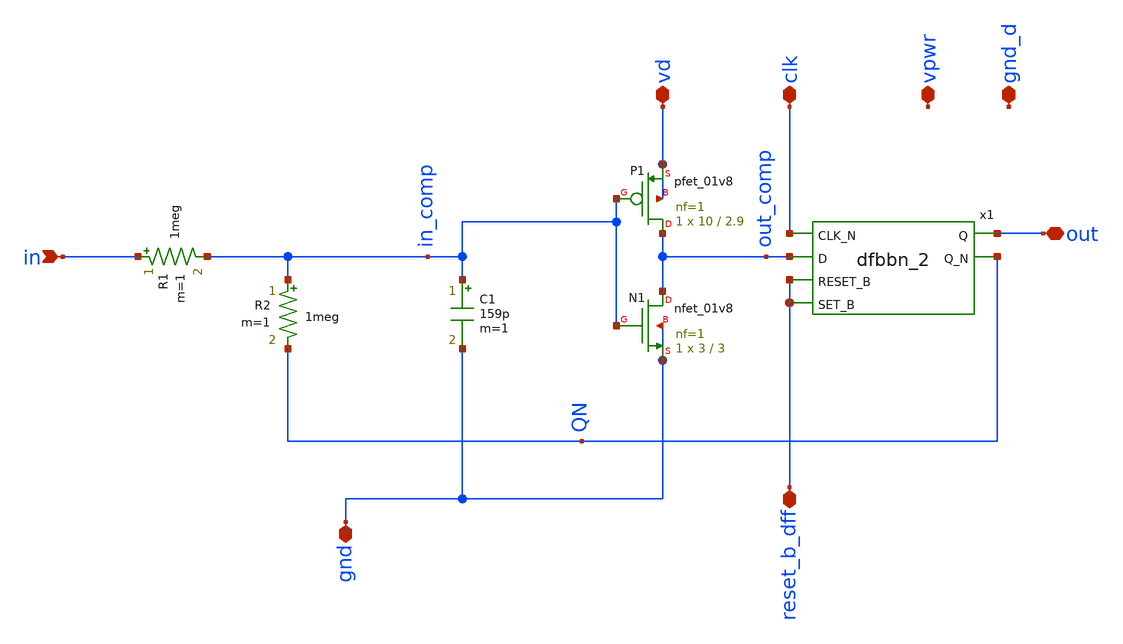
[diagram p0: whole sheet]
** sch_path: mag/sigma-delta_modulator/xschem/sigma-delta-test.sch
* Copyright 2020 Stefan Frederik Schippers
* Licensed under the Apache License, Version 2.0 (the "License");
* you may not use this file except in compliance with the License.
* You may obtain a copy of the License at
* https://www.apache.org/licenses/LICENSE-2.0
* Unless required by applicable law or agreed to in writing, software
* distributed under the License is distributed on an "AS IS" BASIS,
* WITHOUT WARRANTIES OR CONDITIONS OF ANY KIND, either express or implied.
* See the License for the specific language governing permissions and
* limitations under the License.
**.subckt sigma-delta-test in gnd clk out reset_b_dff vpwr gnd_d vd
*.ipin in
*.iopin gnd
*.iopin clk
*.iopin out
*.iopin reset_b_dff
*.iopin vpwr
*.iopin gnd_d
*.iopin vd
XN1 out_comp in_comp gnd gnd sky130_fd_pr__nfet_01v8 L=3 W=3 nf=1 ad='int((nf+1)/2) * W/nf * 0.29' as='int((nf+2)/2) * W/nf * 0.29'
+ pd='2*int((nf+1)/2) * (W/nf + 0.29)' ps='2*int((nf+2)/2) * (W/nf + 0.29)' nrd='0.29 / W' nrs='0.29 / W'
+ sa=0 sb=0 sd=0 mult=1 m=1
XP1 out_comp in_comp vd vd sky130_fd_pr__pfet_01v8 L=2.9 W=10 nf=1 ad='int((nf+1)/2) * W/nf * 0.29' as='int((nf+2)/2) * W/nf * 0.29'
+ pd='2*int((nf+1)/2) * (W/nf + 0.29)' ps='2*int((nf+2)/2) * (W/nf + 0.29)' nrd='0.29 / W' nrs='0.29 / W'
+ sa=0 sb=0 sd=0 mult=1 m=1
R1 in in_comp 1meg m=1
R2 in_comp QN 1meg m=1
C1 in_comp gnd 159p m=1
x1 clk out_comp reset_b_dff reset_b_dff GND GND VD VD out QN sky130_fd_sc_hd__dfbbn_2
**** begin user architecture code




**** end user architecture code
**.ends
.end
